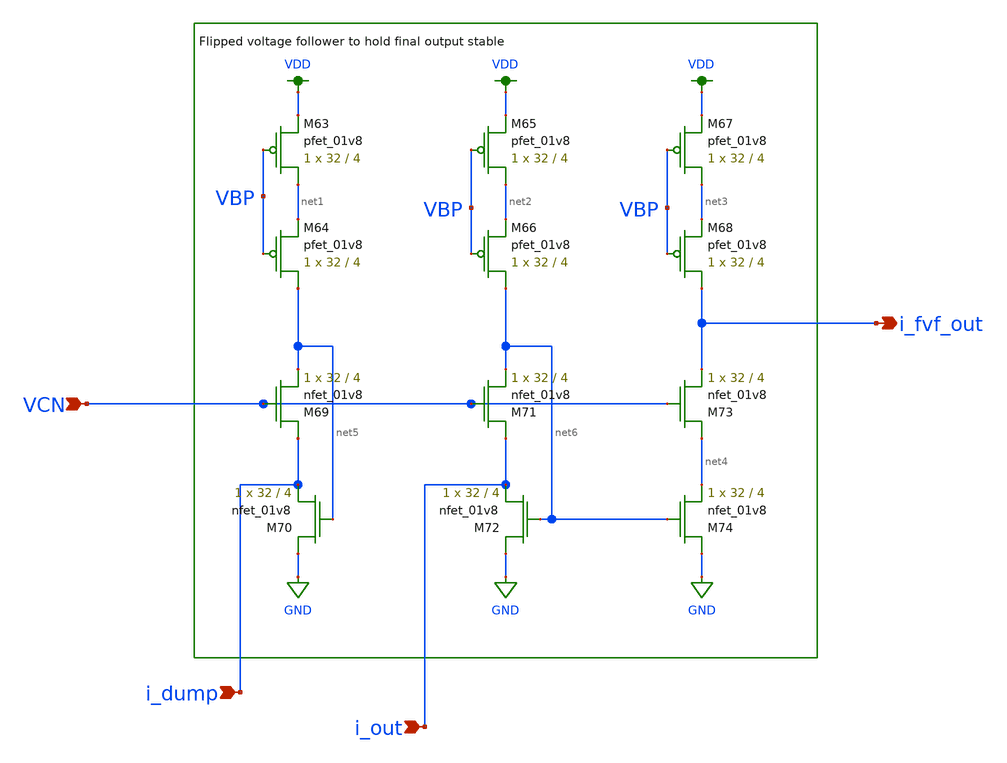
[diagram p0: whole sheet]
** sch_path: schemas/fvf_block.sch
**.subckt fvf_block i_dump i_out VCN i_fvf_out
*.ipin i_dump
*.ipin i_out
*.ipin VCN
*.opin i_fvf_out
XM63 net1 VBP VDD VDD sky130_fd_pr__pfet_01v8 L=4 W=32 nf=1 ad='int((nf+1)/2) * W/nf * 0.29' as='int((nf+2)/2) * W/nf * 0.29'
+ pd='2*int((nf+1)/2) * (W/nf + 0.29)' ps='2*int((nf+2)/2) * (W/nf + 0.29)' nrd='0.29 / W' nrs='0.29 / W'
+ sa=0 sb=0 sd=0 mult=1 m=1
XM64 net5 VBP net1 VDD sky130_fd_pr__pfet_01v8 L=4 W=32 nf=1 ad='int((nf+1)/2) * W/nf * 0.29' as='int((nf+2)/2) * W/nf * 0.29'
+ pd='2*int((nf+1)/2) * (W/nf + 0.29)' ps='2*int((nf+2)/2) * (W/nf + 0.29)' nrd='0.29 / W' nrs='0.29 / W'
+ sa=0 sb=0 sd=0 mult=1 m=1
XM65 net2 VBP VDD VDD sky130_fd_pr__pfet_01v8 L=4 W=32 nf=1 ad='int((nf+1)/2) * W/nf * 0.29' as='int((nf+2)/2) * W/nf * 0.29'
+ pd='2*int((nf+1)/2) * (W/nf + 0.29)' ps='2*int((nf+2)/2) * (W/nf + 0.29)' nrd='0.29 / W' nrs='0.29 / W'
+ sa=0 sb=0 sd=0 mult=1 m=1
XM66 net6 VBP net2 VDD sky130_fd_pr__pfet_01v8 L=4 W=32 nf=1 ad='int((nf+1)/2) * W/nf * 0.29' as='int((nf+2)/2) * W/nf * 0.29'
+ pd='2*int((nf+1)/2) * (W/nf + 0.29)' ps='2*int((nf+2)/2) * (W/nf + 0.29)' nrd='0.29 / W' nrs='0.29 / W'
+ sa=0 sb=0 sd=0 mult=1 m=1
XM67 net3 VBP VDD VDD sky130_fd_pr__pfet_01v8 L=4 W=32 nf=1 ad='int((nf+1)/2) * W/nf * 0.29' as='int((nf+2)/2) * W/nf * 0.29'
+ pd='2*int((nf+1)/2) * (W/nf + 0.29)' ps='2*int((nf+2)/2) * (W/nf + 0.29)' nrd='0.29 / W' nrs='0.29 / W'
+ sa=0 sb=0 sd=0 mult=1 m=1
XM68 i_fvf_out VBP net3 VDD sky130_fd_pr__pfet_01v8 L=4 W=32 nf=1 ad='int((nf+1)/2) * W/nf * 0.29' as='int((nf+2)/2) * W/nf * 0.29'
+ pd='2*int((nf+1)/2) * (W/nf + 0.29)' ps='2*int((nf+2)/2) * (W/nf + 0.29)' nrd='0.29 / W' nrs='0.29 / W'
+ sa=0 sb=0 sd=0 mult=1 m=1
XM69 i_dump VCN net5 GND sky130_fd_pr__nfet_01v8 L=4 W=32 nf=1 ad='int((nf+1)/2) * W/nf * 0.29' as='int((nf+2)/2) * W/nf * 0.29'
+ pd='2*int((nf+1)/2) * (W/nf + 0.29)' ps='2*int((nf+2)/2) * (W/nf + 0.29)' nrd='0.29 / W' nrs='0.29 / W'
+ sa=0 sb=0 sd=0 mult=1 m=1
XM70 GND net5 i_dump GND sky130_fd_pr__nfet_01v8 L=4 W=32 nf=1 ad='int((nf+1)/2) * W/nf * 0.29' as='int((nf+2)/2) * W/nf * 0.29'
+ pd='2*int((nf+1)/2) * (W/nf + 0.29)' ps='2*int((nf+2)/2) * (W/nf + 0.29)' nrd='0.29 / W' nrs='0.29 / W'
+ sa=0 sb=0 sd=0 mult=1 m=1
XM71 i_out VCN net6 GND sky130_fd_pr__nfet_01v8 L=4 W=32 nf=1 ad='int((nf+1)/2) * W/nf * 0.29' as='int((nf+2)/2) * W/nf * 0.29'
+ pd='2*int((nf+1)/2) * (W/nf + 0.29)' ps='2*int((nf+2)/2) * (W/nf + 0.29)' nrd='0.29 / W' nrs='0.29 / W'
+ sa=0 sb=0 sd=0 mult=1 m=1
XM72 GND net6 i_out GND sky130_fd_pr__nfet_01v8 L=4 W=32 nf=1 ad='int((nf+1)/2) * W/nf * 0.29' as='int((nf+2)/2) * W/nf * 0.29'
+ pd='2*int((nf+1)/2) * (W/nf + 0.29)' ps='2*int((nf+2)/2) * (W/nf + 0.29)' nrd='0.29 / W' nrs='0.29 / W'
+ sa=0 sb=0 sd=0 mult=1 m=1
XM73 net4 VCN i_fvf_out GND sky130_fd_pr__nfet_01v8 L=4 W=32 nf=1 ad='int((nf+1)/2) * W/nf * 0.29' as='int((nf+2)/2) * W/nf * 0.29'
+ pd='2*int((nf+1)/2) * (W/nf + 0.29)' ps='2*int((nf+2)/2) * (W/nf + 0.29)' nrd='0.29 / W' nrs='0.29 / W'
+ sa=0 sb=0 sd=0 mult=1 m=1
XM74 GND net6 net4 GND sky130_fd_pr__nfet_01v8 L=4 W=32 nf=1 ad='int((nf+1)/2) * W/nf * 0.29' as='int((nf+2)/2) * W/nf * 0.29'
+ pd='2*int((nf+1)/2) * (W/nf + 0.29)' ps='2*int((nf+2)/2) * (W/nf + 0.29)' nrd='0.29 / W' nrs='0.29 / W'
+ sa=0 sb=0 sd=0 mult=1 m=1
**.ends
.GLOBAL VDD
.GLOBAL GND
.end
